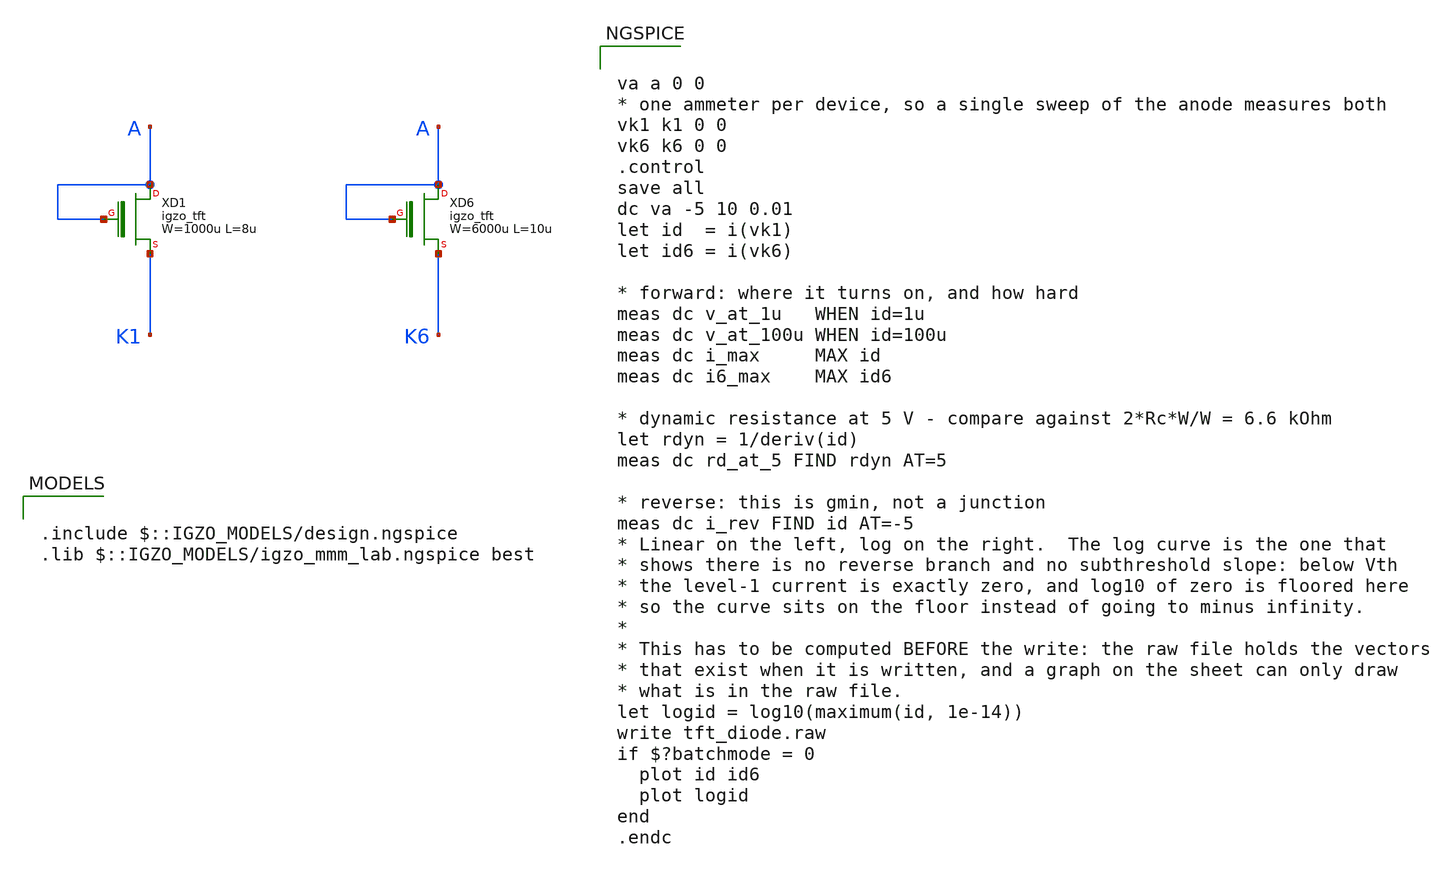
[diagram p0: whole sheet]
** sch_path: libs.tech/xschem/tests/tft_diode.sch
**.subckt tft_diode
XXD1 A A K1 igzo_tft W=1000u L=8u ov=5u nf=1 m=1
XXD6 A A K6 igzo_tft W=6000u L=10u ov=2u nf=1 m=1
**** begin user architecture code

.include $::IGZO_MODELS/design.ngspice
.lib $::IGZO_MODELS/igzo_mmm_lab.ngspice best



va a 0 0
* one ammeter per device, so a single sweep of the anode measures both
vk1 k1 0 0
vk6 k6 0 0
.control
save all
dc va -5 10 0.01
let id  = i(vk1)
let id6 = i(vk6)

* forward: where it turns on, and how hard
meas dc v_at_1u   WHEN id=1u
meas dc v_at_100u WHEN id=100u
meas dc i_max     MAX id
meas dc i6_max    MAX id6

* dynamic resistance at 5 V - compare against 2*Rc*W/W = 6.6 kOhm
let rdyn = 1/deriv(id)
meas dc rd_at_5 FIND rdyn AT=5

* reverse: this is gmin, not a junction
meas dc i_rev FIND id AT=-5
* Linear on the left, log on the right.  The log curve is the one that
* shows there is no reverse branch and no subthreshold slope: below Vth
* the level-1 current is exactly zero, and log10 of zero is floored here
* so the curve sits on the floor instead of going to minus infinity.
*
* This has to be computed BEFORE the write: the raw file holds the vectors
* that exist when it is written, and a graph on the sheet can only draw
* what is in the raw file.
let logid = log10(maximum(id, 1e-14))
write tft_diode.raw
if $?batchmode = 0
  plot id id6
  plot logid
end
.endc


**** end user architecture code
**.ends
.end
